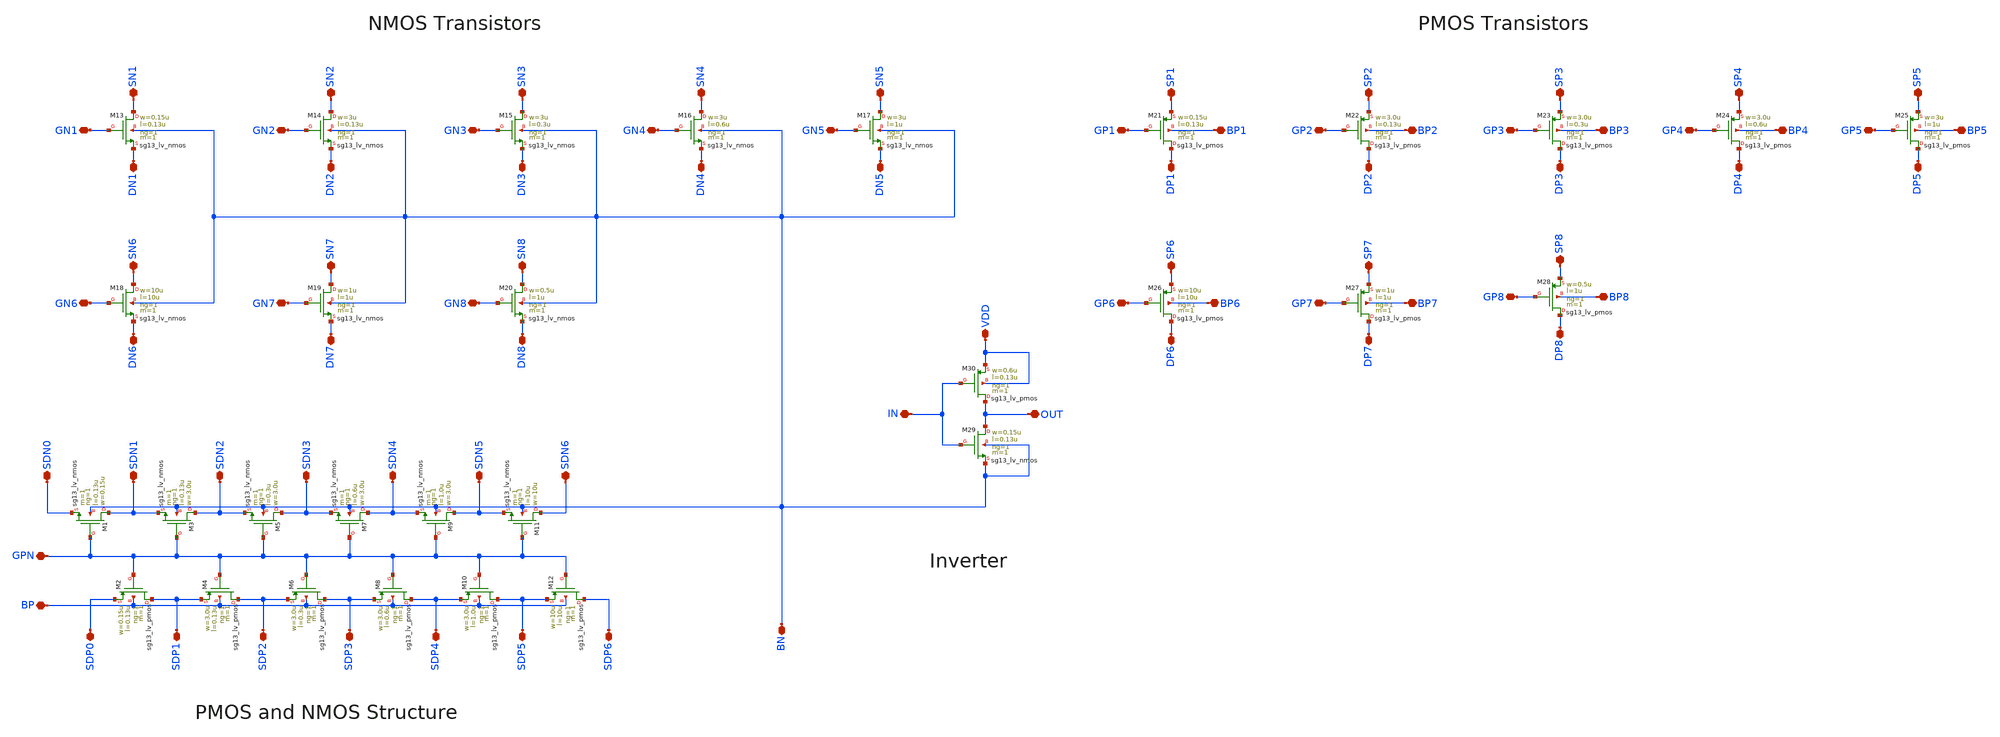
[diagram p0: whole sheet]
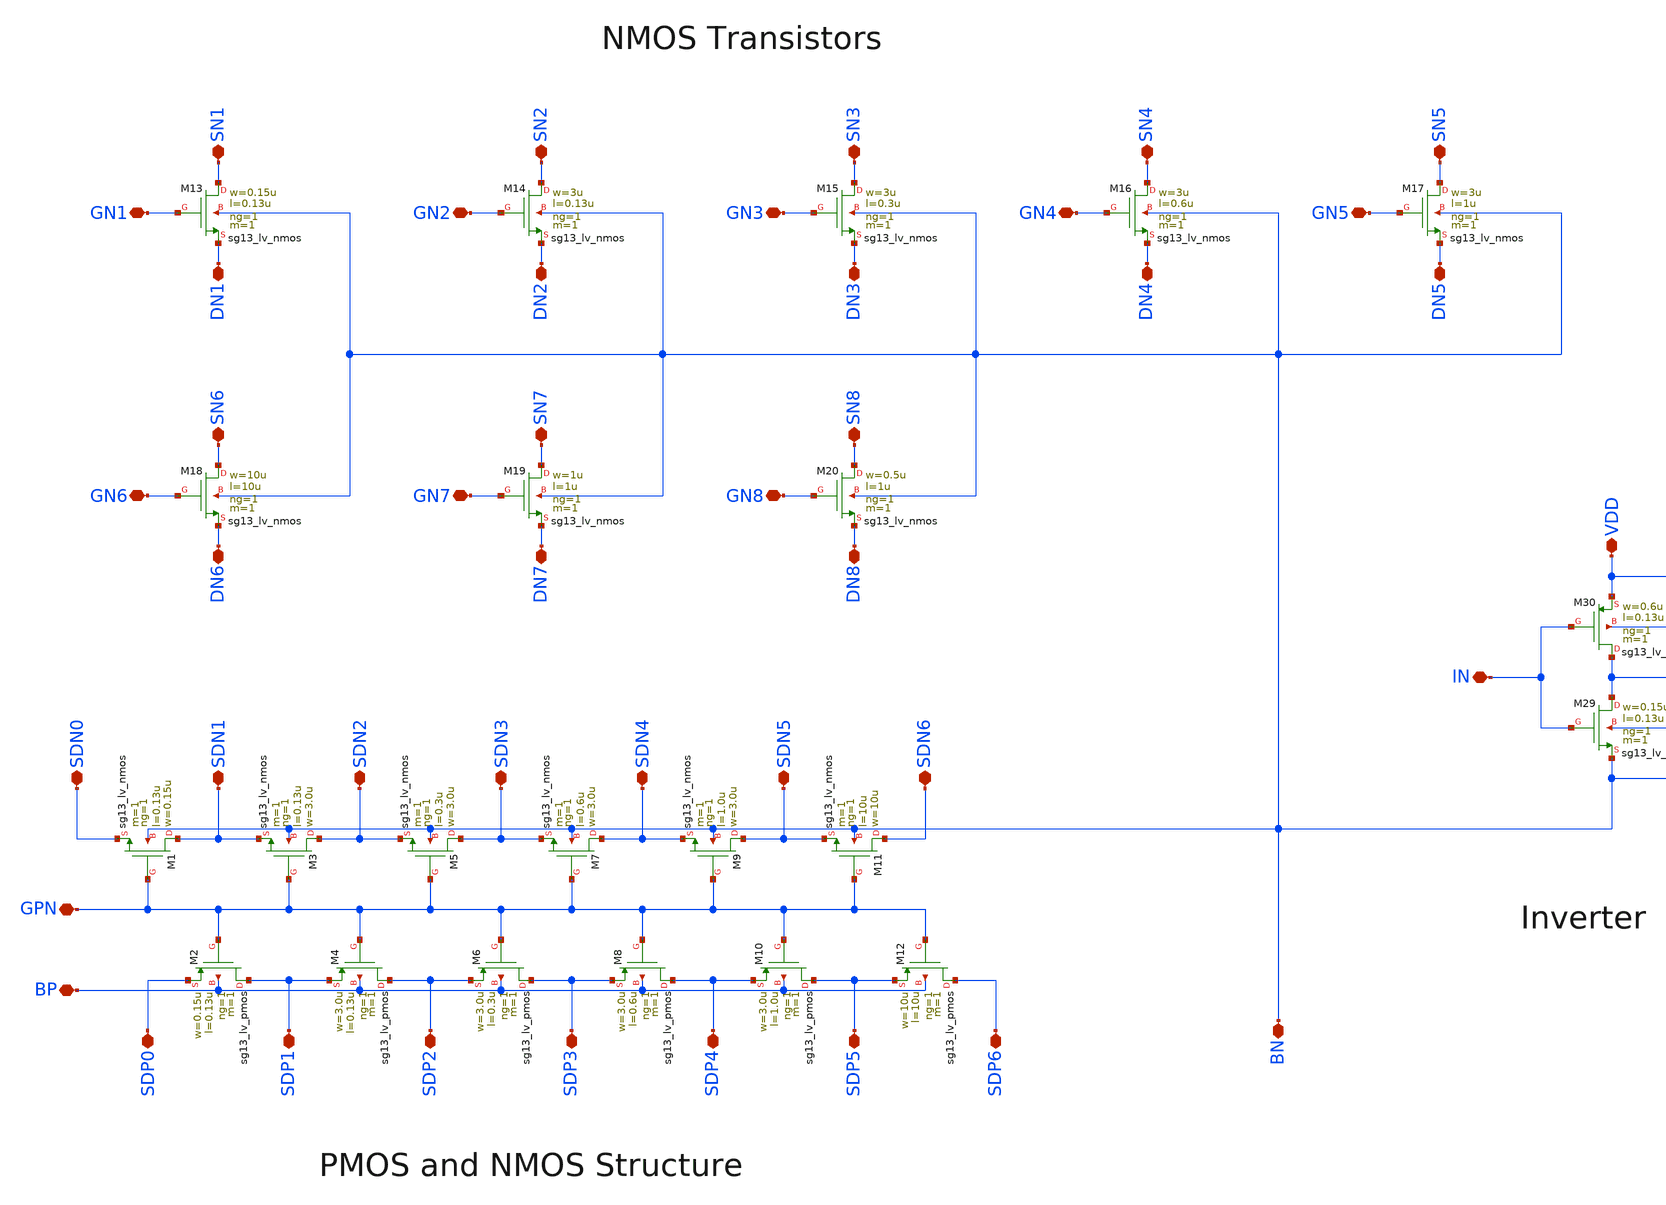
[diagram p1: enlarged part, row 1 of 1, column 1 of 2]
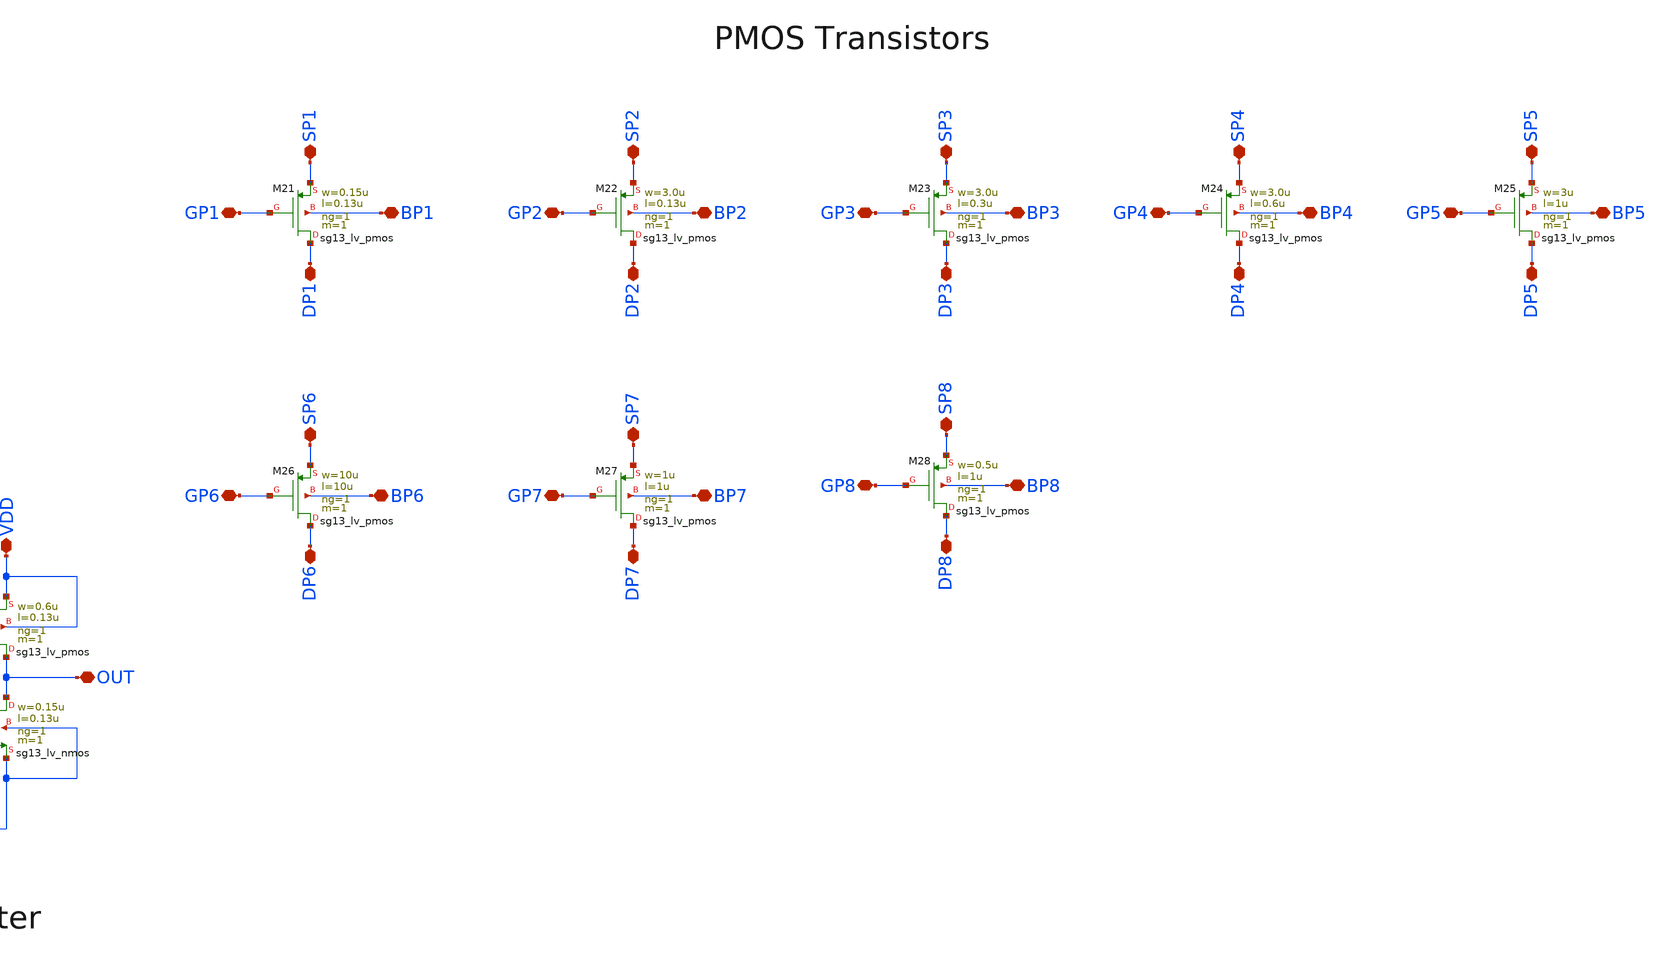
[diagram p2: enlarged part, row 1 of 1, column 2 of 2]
** sch_path: CryoChip/design_data/xschem/CryoChip.sch
**.subckt CryoChip SN1 DN1 GN1 SN2 DN2 GN2 SN3 DN3 GN3 SN4 DN4 GN4 SN5 DN5 GN5 SN6 DN6 GN6 SN7 DN7
*+ GN7 SN8 DN8 GN8 OUT IN VDD BP1 SP1 DP1 GP1 BP2 SP2 DP2 GP2 BP3 SP3 DP3 GP3 BP4 SP4 DP4 GP4 BP5 SP5 DP5
*+ GP5 BP6 SP6 DP6 GP6 BP7 SP7 DP7 GP7 BP8 SP8 DP8 GP8 GPN SDP1 SDP2 SDP3 SDP4 SDP5 SDN5 SDN4 SDN3 SDN2
*+ SDN1 SDN0 SDP6 SDP0 SDN6 BP BN
*.iopin SN1
*.iopin DN1
*.iopin GN1
*.iopin SN2
*.iopin DN2
*.iopin GN2
*.iopin SN3
*.iopin DN3
*.iopin GN3
*.iopin SN4
*.iopin DN4
*.iopin GN4
*.iopin SN5
*.iopin DN5
*.iopin GN5
*.iopin SN6
*.iopin DN6
*.iopin GN6
*.iopin SN7
*.iopin DN7
*.iopin GN7
*.iopin SN8
*.iopin DN8
*.iopin GN8
*.iopin OUT
*.iopin IN
*.iopin VDD
*.iopin BP1
*.iopin SP1
*.iopin DP1
*.iopin GP1
*.iopin BP2
*.iopin SP2
*.iopin DP2
*.iopin GP2
*.iopin BP3
*.iopin SP3
*.iopin DP3
*.iopin GP3
*.iopin BP4
*.iopin SP4
*.iopin DP4
*.iopin GP4
*.iopin BP5
*.iopin SP5
*.iopin DP5
*.iopin GP5
*.iopin BP6
*.iopin SP6
*.iopin DP6
*.iopin GP6
*.iopin BP7
*.iopin SP7
*.iopin DP7
*.iopin GP7
*.iopin BP8
*.iopin SP8
*.iopin DP8
*.iopin GP8
*.iopin GPN
*.iopin SDP1
*.iopin SDP2
*.iopin SDP3
*.iopin SDP4
*.iopin SDP5
*.iopin SDN5
*.iopin SDN4
*.iopin SDN3
*.iopin SDN2
*.iopin SDN1
*.iopin SDN0
*.iopin SDP6
*.iopin SDP0
*.iopin SDN6
*.iopin BP
*.iopin BN
XM13 SN1 GN1 DN1 BN sg13_lv_nmos w=0.15u l=0.13u ng=1 m=1 mm_ok=1
XM14 SN2 GN2 DN2 BN sg13_lv_nmos w=3u l=0.13u ng=1 m=1 mm_ok=1
XM15 SN3 GN3 DN3 BN sg13_lv_nmos w=3u l=0.3u ng=1 m=1 mm_ok=1
XM16 SN4 GN4 DN4 BN sg13_lv_nmos w=3u l=0.6u ng=1 m=1 mm_ok=1
XM17 SN5 GN5 DN5 BN sg13_lv_nmos w=3u l=1u ng=1 m=1 mm_ok=1
XM18 SN6 GN6 DN6 BN sg13_lv_nmos w=10u l=10u ng=1 m=1 mm_ok=1
XM19 SN7 GN7 DN7 BN sg13_lv_nmos w=1u l=1u ng=1 m=1 mm_ok=1
XM20 SN8 GN8 DN8 BN sg13_lv_nmos w=0.5u l=1u ng=1 m=1 mm_ok=1
XM21 DP1 GP1 SP1 BP1 sg13_lv_pmos w=0.15u l=0.13u ng=1 m=1 mm_ok=1
XM22 DP2 GP2 SP2 BP2 sg13_lv_pmos w=3.0u l=0.13u ng=1 m=1 mm_ok=1
XM23 DP3 GP3 SP3 BP3 sg13_lv_pmos w=3.0u l=0.3u ng=1 m=1 mm_ok=1
XM24 DP4 GP4 SP4 BP4 sg13_lv_pmos w=3.0u l=0.6u ng=1 m=1 mm_ok=1
XM25 DP5 GP5 SP5 BP5 sg13_lv_pmos w=3u l=1u ng=1 m=1 mm_ok=1
XM26 DP6 GP6 SP6 BP6 sg13_lv_pmos w=10u l=10u ng=1 m=1 mm_ok=1
XM27 DP7 GP7 SP7 BP7 sg13_lv_pmos w=1u l=1u ng=1 m=1 mm_ok=1
XM28 DP8 GP8 SP8 BP8 sg13_lv_pmos w=0.5u l=1u ng=1 m=1 mm_ok=1
XM29 OUT IN BN BN sg13_lv_nmos w=0.15u l=0.13u ng=1 m=1 mm_ok=1
XM30 OUT IN VDD VDD sg13_lv_pmos w=0.6u l=0.13u ng=1 m=1 mm_ok=1
XM1 SDN1 GPN SDN0 BN sg13_lv_nmos w=0.15u l=0.13u ng=1 m=1 mm_ok=1
XM2 SDP1 GPN SDP0 BP sg13_lv_pmos w=0.15u l=0.13u ng=1 m=1 mm_ok=1
XM3 SDN2 GPN SDN1 BN sg13_lv_nmos w=3.0u l=0.13u ng=1 m=1 mm_ok=1
XM4 SDP2 GPN SDP1 BP sg13_lv_pmos w=3.0u l=0.13u ng=1 m=1 mm_ok=1
XM5 SDN3 GPN SDN2 BN sg13_lv_nmos w=3.0u l=0.3u ng=1 m=1 mm_ok=1
XM6 SDP3 GPN SDP2 BP sg13_lv_pmos w=3.0u l=0.3u ng=1 m=1 mm_ok=1
XM7 SDN4 GPN SDN3 BN sg13_lv_nmos w=3.0u l=0.6u ng=1 m=1 mm_ok=1
XM8 SDP4 GPN SDP3 BP sg13_lv_pmos w=3.0u l=0.6u ng=1 m=1 mm_ok=1
XM9 SDN5 GPN SDN4 BN sg13_lv_nmos w=3.0u l=1.0u ng=1 m=1 mm_ok=1
XM10 SDP5 GPN SDP4 BP sg13_lv_pmos w=3.0u l=1.0u ng=1 m=1 mm_ok=1
XM11 SDN6 GPN SDN5 BN sg13_lv_nmos w=10u l=10u ng=1 m=1 mm_ok=1
XM12 SDP6 GPN SDP5 BP sg13_lv_pmos w=10u l=10u ng=1 m=1 mm_ok=1
**.ends
.end
